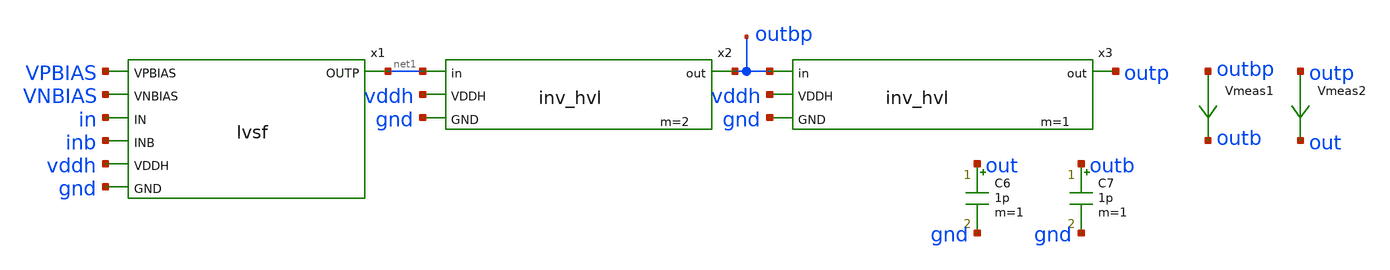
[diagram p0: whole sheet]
** sch_path: xschem/lvsf-tb.sch
.lib $::SKYWATER_MODELS/sky130.lib.spice tt
.include $::SKYWATER_STDCELLS/sky130_fd_sc_hd.spice

**.subckt lvsf-tb
x1 VPBIAS VNBIAS in inb net1 vddh gnd lvsf
C6 out gnd 1p m=1
C7 outb gnd 1p m=1
Vmeas1 outbp outb 0
.save i(vmeas1)
Vmeas2 outp out 0
.save i(vmeas2)
x2 net1 outbp vddh gnd inv_hvl m=2
x3 outbp outp vddh gnd inv_hvl m=1
**** begin user architecture code



  .param max_freq=100e3 period={1/max_freq} time_high={period/2}
  .param delay_vin1={time_high} delay_vin2={time_high*1.5}
  .param lval=100u

  .option wnflag=1
  .option safecurrents

  Vddh vddh gnd dc 5.5
  Vin  in  gnd pulse(0 1.8 {delay_vin1} 1p 1p {time_high} {period})
  Vinb inb gnd pulse(1.8 0 {delay_vin1} 1p 1p {time_high} {period})
  *vin in gnd 1.8
  *vinb inb gnd 0
  *vpb vpbias gnd 1.3273
  vpb vpbias gnd 3.6965
  vnb vnbias gnd 1.354
  *vnb vnbias gnd 1.5
  .control
     reset
     save all
     tran 1n 25u
     *dc vnb 0 5.5 0.01
     write lvsf-tb.raw
     set appendwrite
*    quit 0
  .endc



**** end user architecture code
**.ends

* expanding   symbol:  lvsf.sym # of pins=7
** sym_path: xschem/lvsf.sym
** sch_path: xschem/lvsf.sch
.subckt lvsf VPBIAS VNBIAS IN INB OUTP VDDH GND
*.ipin IN
*.ipin INB
*.opin OUTP
*.ipin VDDH
*.ipin GND
*.ipin VPBIAS
*.ipin VNBIAS
Vmeas net1 net2 0
.save i(vmeas)
XM13 net6 IN GND GND sky130_fd_pr__nfet_01v8 L=0.15 W=3 nf=1 ad='int((nf+1)/2) * W/nf * 0.29' as='int((nf+2)/2) * W/nf * 0.29'
+ pd='2*int((nf+1)/2) * (W/nf + 0.29)' ps='2*int((nf+2)/2) * (W/nf + 0.29)' nrd='0.29 / W' nrs='0.29 / W'
+ sa=0 sb=0 sd=0 mult=1 m=1
XM1 net3 VPBIAS VDDH VDDH sky130_fd_pr__pfet_g5v0d10v5 L=0.8 W=1 nf=1 ad='int((nf+1)/2) * W/nf * 0.29'
+ as='int((nf+2)/2) * W/nf * 0.29' pd='2*int((nf+1)/2) * (W/nf + 0.29)' ps='2*int((nf+2)/2) * (W/nf + 0.29)'
+ nrd='0.29 / W' nrs='0.29 / W' sa=0 sb=0 sd=0 mult=1 m=1
XM2 net1 VPBIAS VDDH VDDH sky130_fd_pr__pfet_g5v0d10v5 L=0.8 W=1 nf=1 ad='int((nf+1)/2) * W/nf * 0.29'
+ as='int((nf+2)/2) * W/nf * 0.29' pd='2*int((nf+1)/2) * (W/nf + 0.29)' ps='2*int((nf+2)/2) * (W/nf + 0.29)'
+ nrd='0.29 / W' nrs='0.29 / W' sa=0 sb=0 sd=0 mult=1 m=1
XM3 OUTPB OUTP net4 VDDH sky130_fd_pr__pfet_g5v0d10v5 L=0.8 W=1 nf=1 ad='int((nf+1)/2) * W/nf * 0.29'
+ as='int((nf+2)/2) * W/nf * 0.29' pd='2*int((nf+1)/2) * (W/nf + 0.29)' ps='2*int((nf+2)/2) * (W/nf + 0.29)'
+ nrd='0.29 / W' nrs='0.29 / W' sa=0 sb=0 sd=0 mult=1 m=1
XM4 OUTP OUTPB net2 VDDH sky130_fd_pr__pfet_g5v0d10v5 L=0.8 W=1 nf=1 ad='int((nf+1)/2) * W/nf * 0.29'
+ as='int((nf+2)/2) * W/nf * 0.29' pd='2*int((nf+1)/2) * (W/nf + 0.29)' ps='2*int((nf+2)/2) * (W/nf + 0.29)'
+ nrd='0.29 / W' nrs='0.29 / W' sa=0 sb=0 sd=0 mult=1 m=1
XM5 OUTPB VNBIAS n1 GND sky130_fd_pr__nfet_g5v0d10v5 L=1 W=1 nf=1 ad='int((nf+1)/2) * W/nf * 0.29' as='int((nf+2)/2) * W/nf * 0.29'
+ pd='2*int((nf+1)/2) * (W/nf + 0.29)' ps='2*int((nf+2)/2) * (W/nf + 0.29)' nrd='0.29 / W' nrs='0.29 / W'
+ sa=0 sb=0 sd=0 mult=1 m=1
XM6 OUTP VNBIAS n2 GND sky130_fd_pr__nfet_g5v0d10v5 L=1 W=1 nf=1 ad='int((nf+1)/2) * W/nf * 0.29' as='int((nf+2)/2) * W/nf * 0.29'
+ pd='2*int((nf+1)/2) * (W/nf + 0.29)' ps='2*int((nf+2)/2) * (W/nf + 0.29)' nrd='0.29 / W' nrs='0.29 / W'
+ sa=0 sb=0 sd=0 mult=1 m=1
Vmeas1 net3 net4 0
.save i(vmeas1)
XM7 net5 INB GND GND sky130_fd_pr__nfet_01v8 L=0.15 W=3 nf=1 ad='int((nf+1)/2) * W/nf * 0.29' as='int((nf+2)/2) * W/nf * 0.29'
+ pd='2*int((nf+1)/2) * (W/nf + 0.29)' ps='2*int((nf+2)/2) * (W/nf + 0.29)' nrd='0.29 / W' nrs='0.29 / W'
+ sa=0 sb=0 sd=0 mult=1 m=1
Vmeas2 n2 net5 0
.save i(vmeas2)
Vmeas3 n1 net6 0
.save i(vmeas3)
.ends


* expanding   symbol:  inv_hvl.sym # of pins=4
** sym_path: xschem/inv_hvl.sym
** sch_path: xschem/inv_hvl.sch
.subckt inv_hvl in out VDDH GND
*.opin out
*.ipin VDDH
*.ipin GND
*.ipin in
.param wp=0.84 wn=0.42 l=0.5
XM1 out in VDDH VDDH sky130_fd_pr__pfet_g5v0d10v5 L=l W=wp nf=1 ad='int((nf+1)/2) * W/nf * 0.29' as='int((nf+2)/2) * W/nf * 0.29'
+ pd='2*int((nf+1)/2) * (W/nf + 0.29)' ps='2*int((nf+2)/2) * (W/nf + 0.29)' nrd='0.29 / W' nrs='0.29 / W'
+ sa=0 sb=0 sd=0 mult=m m=m
XM2 out in GND GND sky130_fd_pr__nfet_g5v0d10v5 L=l W=wn nf=1 ad='int((nf+1)/2) * W/nf * 0.29' as='int((nf+2)/2) * W/nf * 0.29'
+ pd='2*int((nf+1)/2) * (W/nf + 0.29)' ps='2*int((nf+2)/2) * (W/nf + 0.29)' nrd='0.29 / W' nrs='0.29 / W'
+ sa=0 sb=0 sd=0 mult=m m=m
.ends

.end
